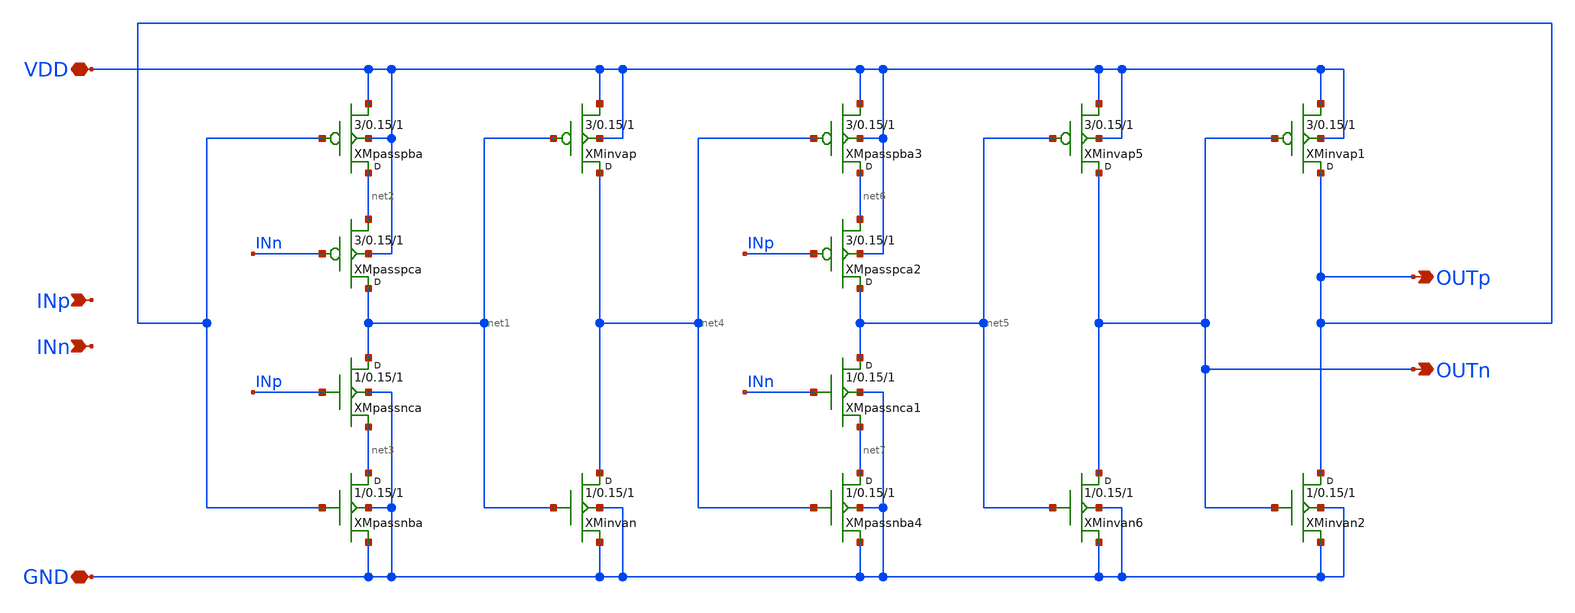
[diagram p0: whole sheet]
** sch_path: design/divider_ff/divider_ff.sch
**.subckt divider_ff INn OUTp VDD GND OUTn INp
*.ipin INn
*.opin OUTp
*.iopin VDD
*.iopin GND
*.opin OUTn
*.ipin INp
XMpassnca net1 INp net3 GND sky130_fd_pr__nfet_01v8 w=1 l=0.15 m=1
XMpasspca net1 INn net2 VDD sky130_fd_pr__pfet_01v8 w=3 l=0.15 m=1
XMpasspba net2 OUTp VDD VDD sky130_fd_pr__pfet_01v8 w=3 l=0.15 m=1
XMpassnba net3 OUTp GND GND sky130_fd_pr__nfet_01v8 w=1 l=0.15 m=1
XMinvap net4 net1 VDD VDD sky130_fd_pr__pfet_01v8 w=3 l=0.15 m=1
XMinvan net4 net1 GND GND sky130_fd_pr__nfet_01v8 w=1 l=0.15 m=1
XMpassnca1 net5 INn net7 GND sky130_fd_pr__nfet_01v8 w=1 l=0.15 m=1
XMpasspca2 net5 INp net6 VDD sky130_fd_pr__pfet_01v8 w=3 l=0.15 m=1
XMpasspba3 net6 net4 VDD VDD sky130_fd_pr__pfet_01v8 w=3 l=0.15 m=1
XMpassnba4 net7 net4 GND GND sky130_fd_pr__nfet_01v8 w=1 l=0.15 m=1
XMinvap5 OUTn net5 VDD VDD sky130_fd_pr__pfet_01v8 w=3 l=0.15 m=1
XMinvan6 OUTn net5 GND GND sky130_fd_pr__nfet_01v8 w=1 l=0.15 m=1
XMinvap1 OUTp OUTn VDD VDD sky130_fd_pr__pfet_01v8 w=3 l=0.15 m=1
XMinvan2 OUTp OUTn GND GND sky130_fd_pr__nfet_01v8 w=1 l=0.15 m=1
**.ends
.end
